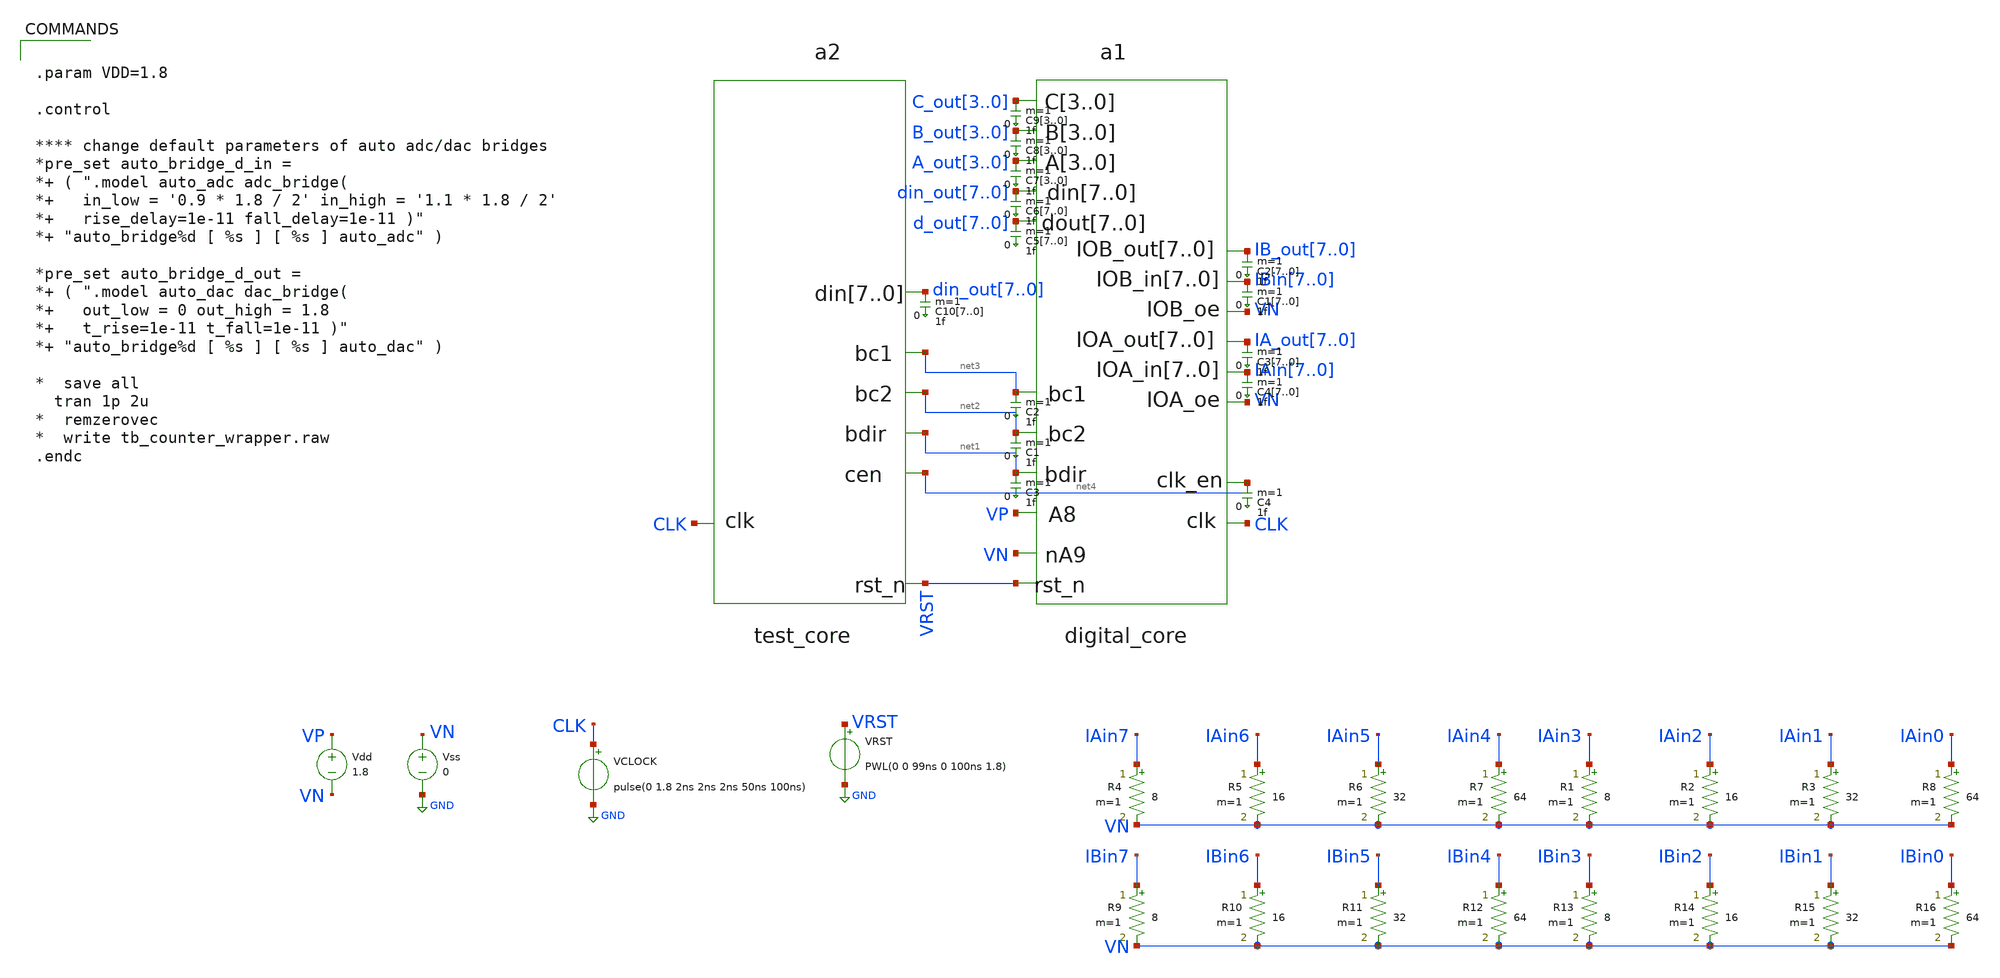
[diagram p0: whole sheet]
** sch_path: xschem/testbench.sch
**.subckt testbench
a1 [ VRST CLK net4 net1 net3 net2 din_out7 din_out6 din_out5 din_out4 din_out3 din_out2 din_out1
+ din_out0 IAin7 IAin6 IAin5 IAin4 IAin3 IAin2 IAin1 IAin0 IBin7 IBin6 IBin5 IBin4 IBin3 IBin2 IBin1 IBin0 VN
+ VP ] [ d_out7 d_out6 d_out5 d_out4 d_out3 d_out2 d_out1 d_out0 IA_out7 IA_out6 IA_out5 IA_out4 IA_out3
+ IA_out2 IA_out1 IA_out0 VN IB_out7 IB_out6 IB_out5 IB_out4 IB_out3 IB_out2 IB_out1 IB_out0 VN ]
+ digital_core
a2 [ CLK VRST ] [ net4 net1 net3 net2 din_out7 din_out6 din_out5 din_out4 din_out3 din_out2 din_out1
+ din_out0 ] test_core
Vdd VP VN 1.8
Vss VN GND 0
R4 IAin7 VN 8 m=1
R5 IAin6 VN 16 m=1
R6 IAin5 VN 32 m=1
R7 IAin4 VN 64 m=1
R1 IAin3 VN 8 m=1
R2 IAin2 VN 16 m=1
R3 IAin1 VN 32 m=1
R8 IAin0 VN 64 m=1
R9 IBin7 VN 8 m=1
R10 IBin6 VN 16 m=1
R11 IBin5 VN 32 m=1
R12 IBin4 VN 64 m=1
R13 IBin3 VN 8 m=1
R14 IBin2 VN 16 m=1
R15 IBin1 VN 32 m=1
R16 IBin0 VN 64 m=1
VCLOCK CLK GND pulse(0 1.8 2ns 2ns 2ns 50ns 100ns)
VRST VRST GND PWL(0 0 99ns 0 100ns 1.8)
C27 IB_out7 0 1f m=1
C26 IB_out6 0 1f m=1
C25 IB_out5 0 1f m=1
C24 IB_out4 0 1f m=1
C23 IB_out3 0 1f m=1
C22 IB_out2 0 1f m=1
C21 IB_out1 0 1f m=1
C20 IB_out0 0 1f m=1
C17 IBin7 0 1f m=1
C16 IBin6 0 1f m=1
C15 IBin5 0 1f m=1
C14 IBin4 0 1f m=1
C13 IBin3 0 1f m=1
C12 IBin2 0 1f m=1
C11 IBin1 0 1f m=1
C10 IBin0 0 1f m=1
C37 IA_out7 0 1f m=1
C36 IA_out6 0 1f m=1
C35 IA_out5 0 1f m=1
C34 IA_out4 0 1f m=1
C33 IA_out3 0 1f m=1
C32 IA_out2 0 1f m=1
C31 IA_out1 0 1f m=1
C30 IA_out0 0 1f m=1
C47 IAin7 0 1f m=1
C46 IAin6 0 1f m=1
C45 IAin5 0 1f m=1
C44 IAin4 0 1f m=1
C43 IAin3 0 1f m=1
C42 IAin2 0 1f m=1
C41 IAin1 0 1f m=1
C40 IAin0 0 1f m=1
C57 d_out7 0 1f m=1
C56 d_out6 0 1f m=1
C55 d_out5 0 1f m=1
C54 d_out4 0 1f m=1
C53 d_out3 0 1f m=1
C52 d_out2 0 1f m=1
C51 d_out1 0 1f m=1
C50 d_out0 0 1f m=1
C67 din_out7 0 1f m=1
C66 din_out6 0 1f m=1
C65 din_out5 0 1f m=1
C64 din_out4 0 1f m=1
C63 din_out3 0 1f m=1
C62 din_out2 0 1f m=1
C61 din_out1 0 1f m=1
C60 din_out0 0 1f m=1
C73 A_out3 0 1f m=1
C72 A_out2 0 1f m=1
C71 A_out1 0 1f m=1
C70 A_out0 0 1f m=1
C83 B_out3 0 1f m=1
C82 B_out2 0 1f m=1
C81 B_out1 0 1f m=1
C80 B_out0 0 1f m=1
C93 C_out3 0 1f m=1
C92 C_out2 0 1f m=1
C91 C_out1 0 1f m=1
C90 C_out0 0 1f m=1
C107 din_out7 0 1f m=1
C106 din_out6 0 1f m=1
C105 din_out5 0 1f m=1
C104 din_out4 0 1f m=1
C103 din_out3 0 1f m=1
C102 din_out2 0 1f m=1
C101 din_out1 0 1f m=1
C100 din_out0 0 1f m=1
C2 net3 0 1f m=1
C1 net2 0 1f m=1
C3 net1 0 1f m=1
C4 net4 0 1f m=1
**** begin user architecture code


.param VDD=1.8

.control

**** change default parameters of auto adc/dac bridges
*pre_set auto_bridge_d_in =
*+ ( ".model auto_adc adc_bridge(
*+   in_low = '0.9 * 1.8 / 2' in_high = '1.1 * 1.8 / 2'
*+   rise_delay=1e-11 fall_delay=1e-11 )"
*+ "auto_bridge%d [ %s ] [ %s ] auto_adc" )

*pre_set auto_bridge_d_out =
*+ ( ".model auto_dac dac_bridge(
*+   out_low = 0 out_high = 1.8
*+   t_rise=1e-11 t_fall=1e-11 )"
*+ "auto_bridge%d [ %s ] [ %s ] auto_dac" )

*  save all
  tran 1p 2u
*  remzerovec
*  write tb_counter_wrapper.raw
.endc


**** end user architecture code
**.ends
.GLOBAL GND
**** begin user architecture code
.model test_core d_cosim simulation="ivlng" sim_args=["test_core"] delay=1e-12
.model digital_core d_cosim simulation="ivlng" sim_args=["digital_core"]
**** end user architecture code
.end
